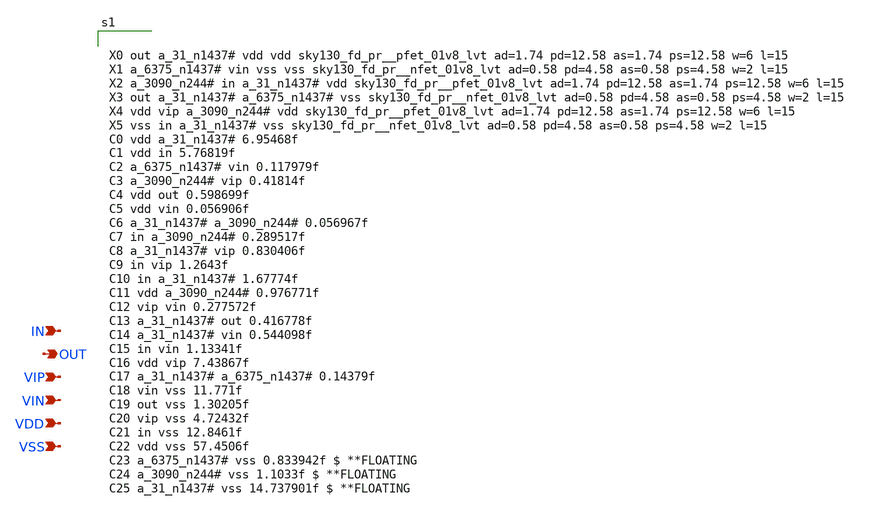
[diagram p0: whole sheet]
** sch_path: top/delay_element_post.sch
**.subckt delay_element_post VDD VIN IN VSS OUT VIP
*.ipin VDD
*.ipin VIN
*.ipin IN
*.ipin VSS
*.opin OUT
*.ipin VIP
**** begin user architecture code


X0 out a_31_n1437# vdd vdd sky130_fd_pr__pfet_01v8_lvt ad=1.74 pd=12.58 as=1.74 ps=12.58 w=6 l=15
X1 a_6375_n1437# vin vss vss sky130_fd_pr__nfet_01v8_lvt ad=0.58 pd=4.58 as=0.58 ps=4.58 w=2 l=15
X2 a_3090_n244# in a_31_n1437# vdd sky130_fd_pr__pfet_01v8_lvt ad=1.74 pd=12.58 as=1.74 ps=12.58 w=6
+ l=15
X3 out a_31_n1437# a_6375_n1437# vss sky130_fd_pr__nfet_01v8_lvt ad=0.58 pd=4.58 as=0.58 ps=4.58 w=2
+ l=15
X4 vdd vip a_3090_n244# vdd sky130_fd_pr__pfet_01v8_lvt ad=1.74 pd=12.58 as=1.74 ps=12.58 w=6 l=15
X5 vss in a_31_n1437# vss sky130_fd_pr__nfet_01v8_lvt ad=0.58 pd=4.58 as=0.58 ps=4.58 w=2 l=15
C0 vdd a_31_n1437# 6.95468f
C1 vdd in 5.76819f
C2 a_6375_n1437# vin 0.117979f
C3 a_3090_n244# vip 0.41814f
C4 vdd out 0.598699f
C5 vdd vin 0.056906f
C6 a_31_n1437# a_3090_n244# 0.056967f
C7 in a_3090_n244# 0.289517f
C8 a_31_n1437# vip 0.830406f
C9 in vip 1.2643f
C10 in a_31_n1437# 1.67774f
C11 vdd a_3090_n244# 0.976771f
C12 vip vin 0.277572f
C13 a_31_n1437# out 0.416778f
C14 a_31_n1437# vin 0.544098f
C15 in vin 1.13341f
C16 vdd vip 7.43867f
C17 a_31_n1437# a_6375_n1437# 0.14379f
C18 vin vss 11.771f
C19 out vss 1.30205f
C20 vip vss 4.72432f
C21 in vss 12.8461f
C22 vdd vss 57.4506f
C23 a_6375_n1437# vss 0.833942f $ **FLOATING
C24 a_3090_n244# vss 1.1033f $ **FLOATING
C25 a_31_n1437# vss 14.737901f $ **FLOATING


C0 a_31_n1616# vin 0.963147f
C1 in vin 1.12606f
C2 a_31_n1616# a_6375_n1616# 0.169373f
C3 vdd vip 7.433569f
C4 vdd a_31_n1616# 6.8485f
C5 vdd in 5.96514f
C6 a_6375_n1616# vin 0.117979f
C7 a_3090_n244# vip 0.41814f
C8 vdd out 0.585541f
C9 vdd vin 0.035251f
C10 a_31_n1616# a_3090_n244# 0.020764f
C11 in a_3090_n244# 0.289501f
C12 a_31_n1616# vip 0.202383f
C13 in vip 1.35686f
C14 in a_31_n1616# 3.37637f
C15 vdd a_3090_n244# 0.977304f
C16 vip vin 0.217406f
C17 a_31_n1616# out 0.479286f
C18 vin vss 11.7144f
C19 out vss 1.23774f
C20 vip vss 4.93206f
C21 in vss 13.5862f
C22 vdd vss 57.480606f
C23 a_6375_n1616# vss 0.825713f $ **FLOATING
C24 a_3090_n244# vss 1.12016f $ **FLOATING
C25 a_31_n1616# vss 15.8812f $ **FLOATING

**** end user architecture code
**.ends
.end
